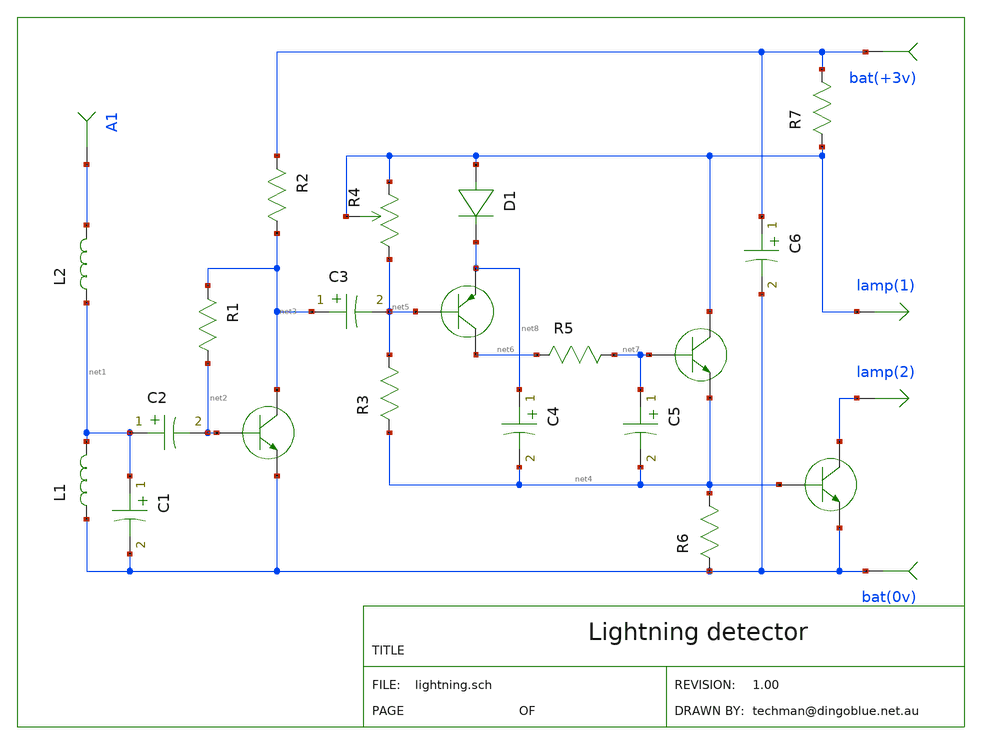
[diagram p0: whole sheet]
** sch_path: xschem-src/xschem_library/gschem_import/lightning.sch
* Copyright (C) 1998-2026 Stefan Frederik Schippers
* This program is free software; you can redistribute it and/or modify
* it under the terms of the GNU General Public License as published by
* the Free Software Foundation; either version 2 of the License, or
* (at your option) any later version.
* This program is distributed in the hope that it will be useful,
* but WITHOUT ANY WARRANTY; without even the implied warranty of
* MERCHANTABILITY or FITNESS FOR A PARTICULAR PURPOSE.  See the
* GNU General Public License for more details.
* You should have received a copy of the GNU General Public License
* along with this program; if not, write to the Free Software
**.subckt lightning lamp(1) lamp(2) bat(+3v) bat(0v) A1
L1 bat(0v) net1 10mH
L2 net1 A1 10mH
C2 net1 net2 0.01uF
C1 net1 bat(0v) 680pf
C3 net3 net5 .01uF
C4 net8 net4 100uF
C5 net7 net4 .005uF
R1 net3 net2 180k
R2 bat(+3v) net3 3.9k
R7 lamp(1) bat(+3v) 47R
R3 net4 net5 22k
R5 net6 net7 2.2K
R6 bat(0v) net4 2.7k
R4 net5 lamp(1) lamp(1) 20k
C6 bat(+3v) bat(0v) 1uF
D1 lamp(1) net8 1N914
Q1 net3 net2 bat(0v) 2N4401
Q2 net6 net5 net8 2N4403
Q3 lamp(1) net7 net4 2N4401
Q4 lamp(2) net4 bat(0v) 2N4401
**.ends
.end
